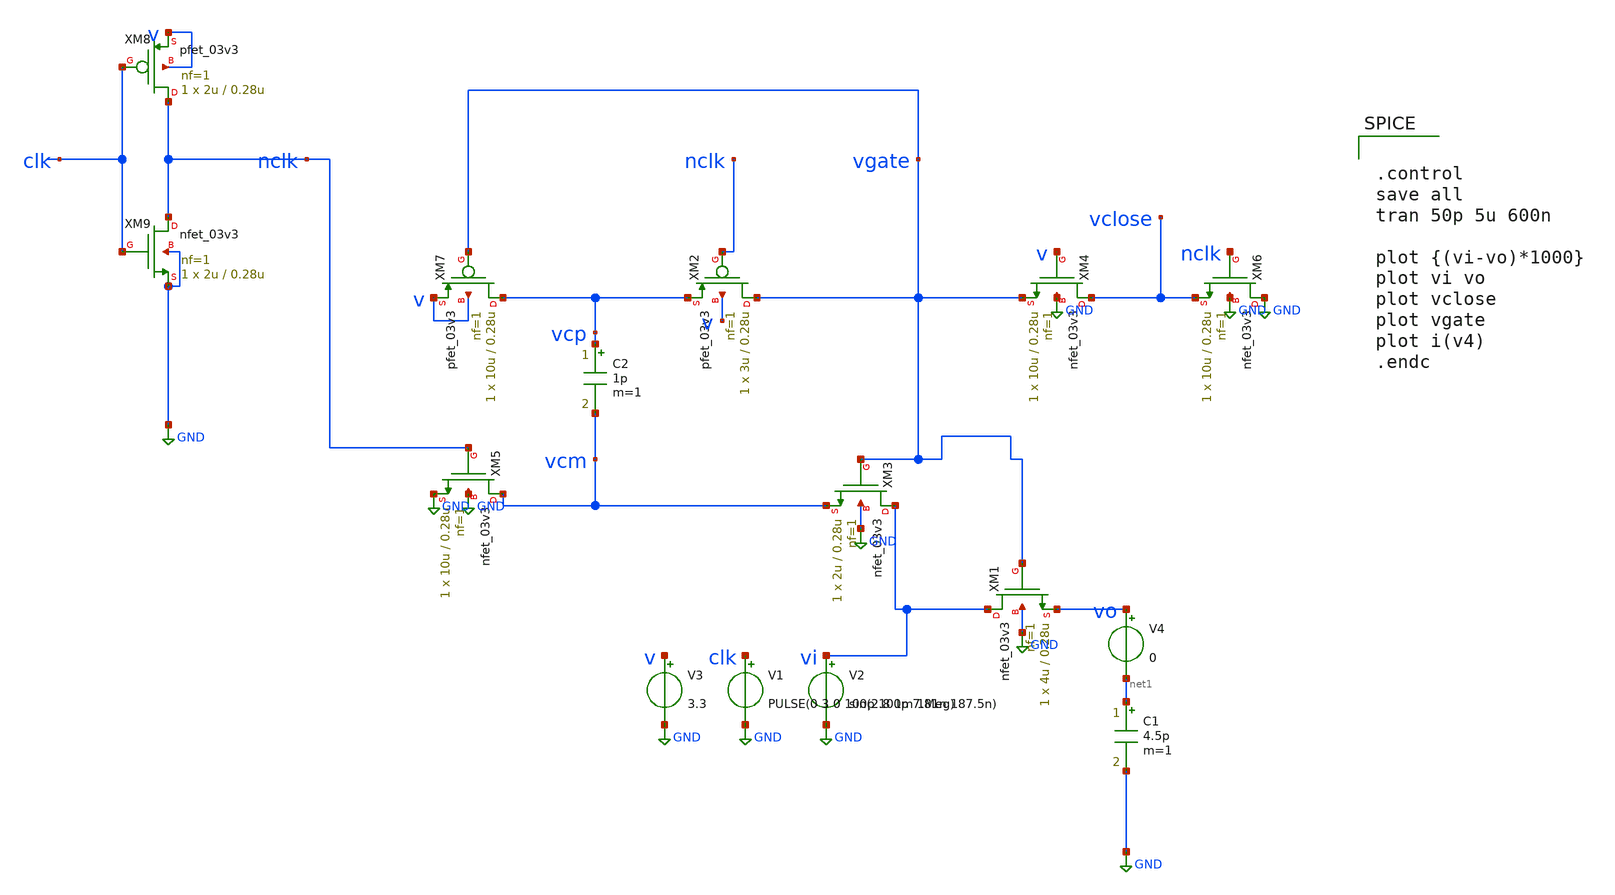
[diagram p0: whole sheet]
** sch_path: SAR_ADC/xschem/test/bootstrap_tb/sin_1m_tb.sch
**.subckt sin_1m_tb
XM1 vi vgate vo GND nfet_03v3 L=0.28u W=4u nf=1 ad='int((nf+1)/2) * W/nf * 0.18u' as='int((nf+2)/2) * W/nf * 0.18u'
+ pd='2*int((nf+1)/2) * (W/nf + 0.18u)' ps='2*int((nf+2)/2) * (W/nf + 0.18u)' nrd='0.18u / W' nrs='0.18u / W'
+ sa=0 sb=0 sd=0 m=1
XM2 vgate nclk vcp v pfet_03v3 L=0.28u W=3u nf=1 ad='int((nf+1)/2) * W/nf * 0.18u' as='int((nf+2)/2) * W/nf * 0.18u'
+ pd='2*int((nf+1)/2) * (W/nf + 0.18u)' ps='2*int((nf+2)/2) * (W/nf + 0.18u)' nrd='0.18u / W' nrs='0.18u / W'
+ sa=0 sb=0 sd=0 m=1
XM3 vi vgate vcm GND nfet_03v3 L=0.28u W=2u nf=1 ad='int((nf+1)/2) * W/nf * 0.18u' as='int((nf+2)/2) * W/nf * 0.18u'
+ pd='2*int((nf+1)/2) * (W/nf + 0.18u)' ps='2*int((nf+2)/2) * (W/nf + 0.18u)' nrd='0.18u / W' nrs='0.18u / W'
+ sa=0 sb=0 sd=0 m=1
XM4 vclose v vgate GND nfet_03v3 L=0.28u W=10u nf=1 ad='int((nf+1)/2) * W/nf * 0.18u' as='int((nf+2)/2) * W/nf * 0.18u'
+ pd='2*int((nf+1)/2) * (W/nf + 0.18u)' ps='2*int((nf+2)/2) * (W/nf + 0.18u)' nrd='0.18u / W' nrs='0.18u / W'
+ sa=0 sb=0 sd=0 m=1
XM5 vcm nclk GND GND nfet_03v3 L=0.28u W=10u nf=1 ad='int((nf+1)/2) * W/nf * 0.18u' as='int((nf+2)/2) * W/nf * 0.18u'
+ pd='2*int((nf+1)/2) * (W/nf + 0.18u)' ps='2*int((nf+2)/2) * (W/nf + 0.18u)' nrd='0.18u / W' nrs='0.18u / W'
+ sa=0 sb=0 sd=0 m=1
XM6 GND nclk vclose GND nfet_03v3 L=0.28u W=10u nf=1 ad='int((nf+1)/2) * W/nf * 0.18u' as='int((nf+2)/2) * W/nf * 0.18u'
+ pd='2*int((nf+1)/2) * (W/nf + 0.18u)' ps='2*int((nf+2)/2) * (W/nf + 0.18u)' nrd='0.18u / W' nrs='0.18u / W'
+ sa=0 sb=0 sd=0 m=1
XM7 vcp vgate v v pfet_03v3 L=0.28u W=10u nf=1 ad='int((nf+1)/2) * W/nf * 0.18u' as='int((nf+2)/2) * W/nf * 0.18u'
+ pd='2*int((nf+1)/2) * (W/nf + 0.18u)' ps='2*int((nf+2)/2) * (W/nf + 0.18u)' nrd='0.18u / W' nrs='0.18u / W'
+ sa=0 sb=0 sd=0 m=1
V2 vi GND sin(2.8 1m 1Meg)
V3 v GND 3.3
XM8 nclk clk v v pfet_03v3 L=0.28u W=2u nf=1 ad='int((nf+1)/2) * W/nf * 0.18u' as='int((nf+2)/2) * W/nf * 0.18u'
+ pd='2*int((nf+1)/2) * (W/nf + 0.18u)' ps='2*int((nf+2)/2) * (W/nf + 0.18u)' nrd='0.18u / W' nrs='0.18u / W'
+ sa=0 sb=0 sd=0 m=1
XM9 nclk clk GND GND nfet_03v3 L=0.28u W=2u nf=1 ad='int((nf+1)/2) * W/nf * 0.18u' as='int((nf+2)/2) * W/nf * 0.18u'
+ pd='2*int((nf+1)/2) * (W/nf + 0.18u)' ps='2*int((nf+2)/2) * (W/nf + 0.18u)' nrd='0.18u / W' nrs='0.18u / W'
+ sa=0 sb=0 sd=0 m=1
C1 net1 GND 4.5p m=1
C2 vcp vcm 1p m=1
V1 clk GND PULSE(0 3 0 100p 100p 7.81n 187.5n)
V4 vo net1 0
**** begin user architecture code


.control
save all
tran 50p 5u 600n

plot {(vi-vo)*1000}
plot vi vo
plot vclose
plot vgate
plot i(v4)
.endc


.include /foss/pdks/gf180mcuC/libs.tech/ngspice/design.ngspice
.lib /foss/pdks/gf180mcuC/libs.tech/ngspice/sm141064.ngspice typical
.lib /foss/pdks/gf180mcuC/libs.tech/ngspice/sm141064.ngspice mimcap_statistical
.lib /foss/pdks/gf180mcuC/libs.tech/ngspice/sm141064.ngspice cap_mim

**** end user architecture code
**.ends
.GLOBAL GND
.end
